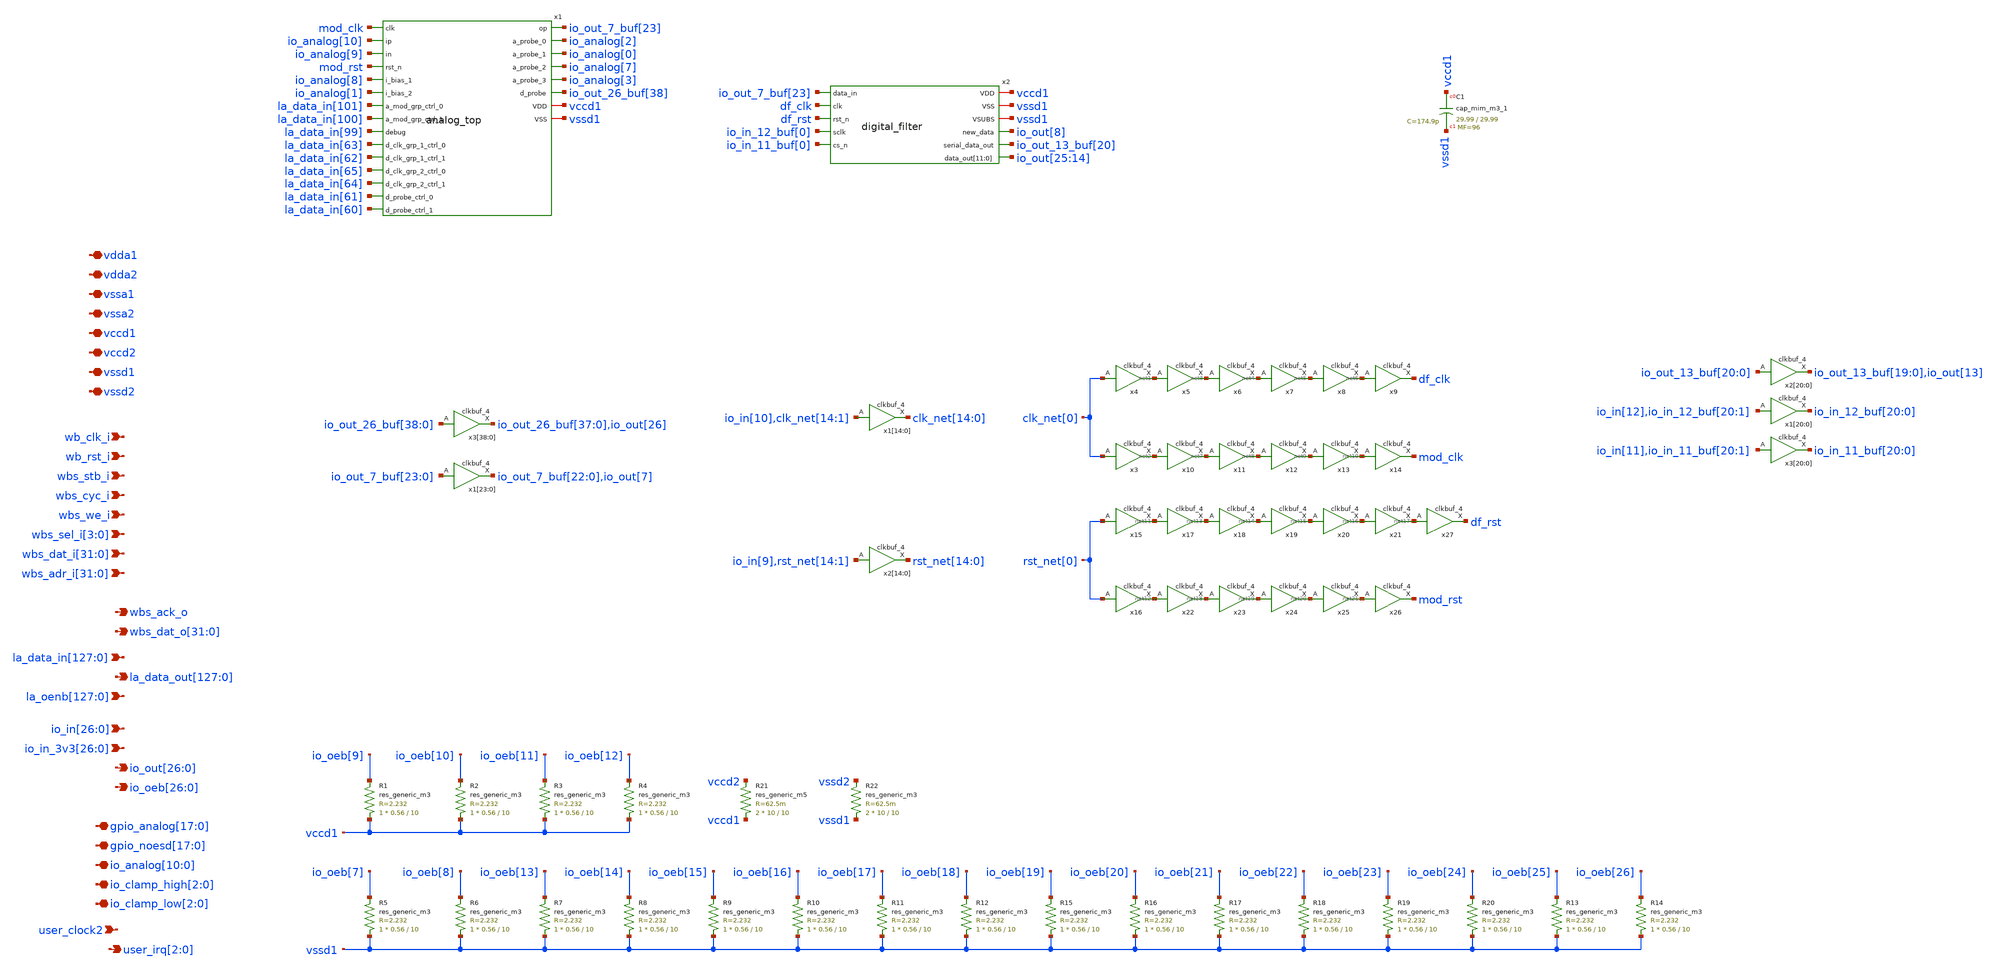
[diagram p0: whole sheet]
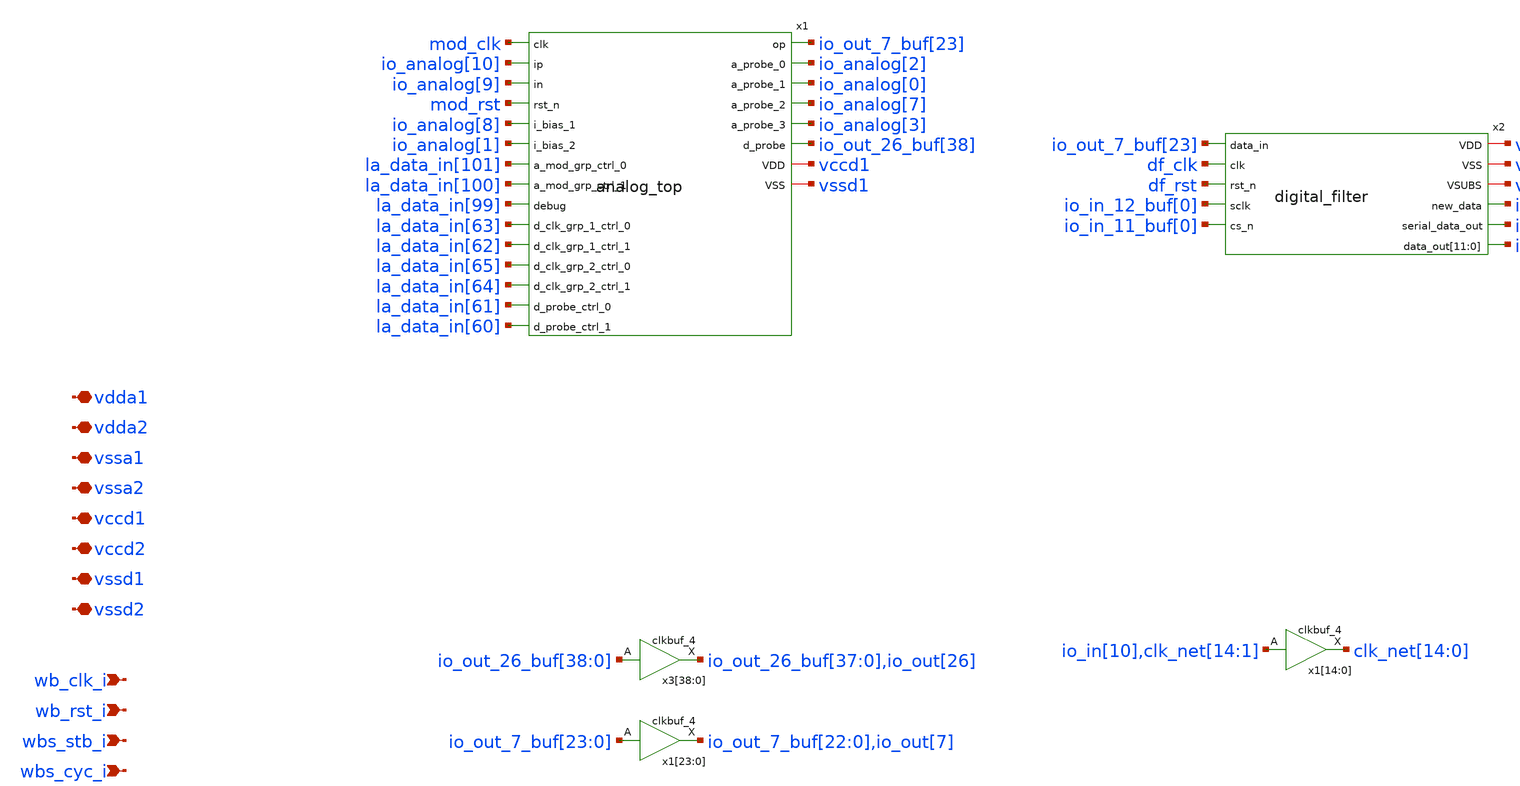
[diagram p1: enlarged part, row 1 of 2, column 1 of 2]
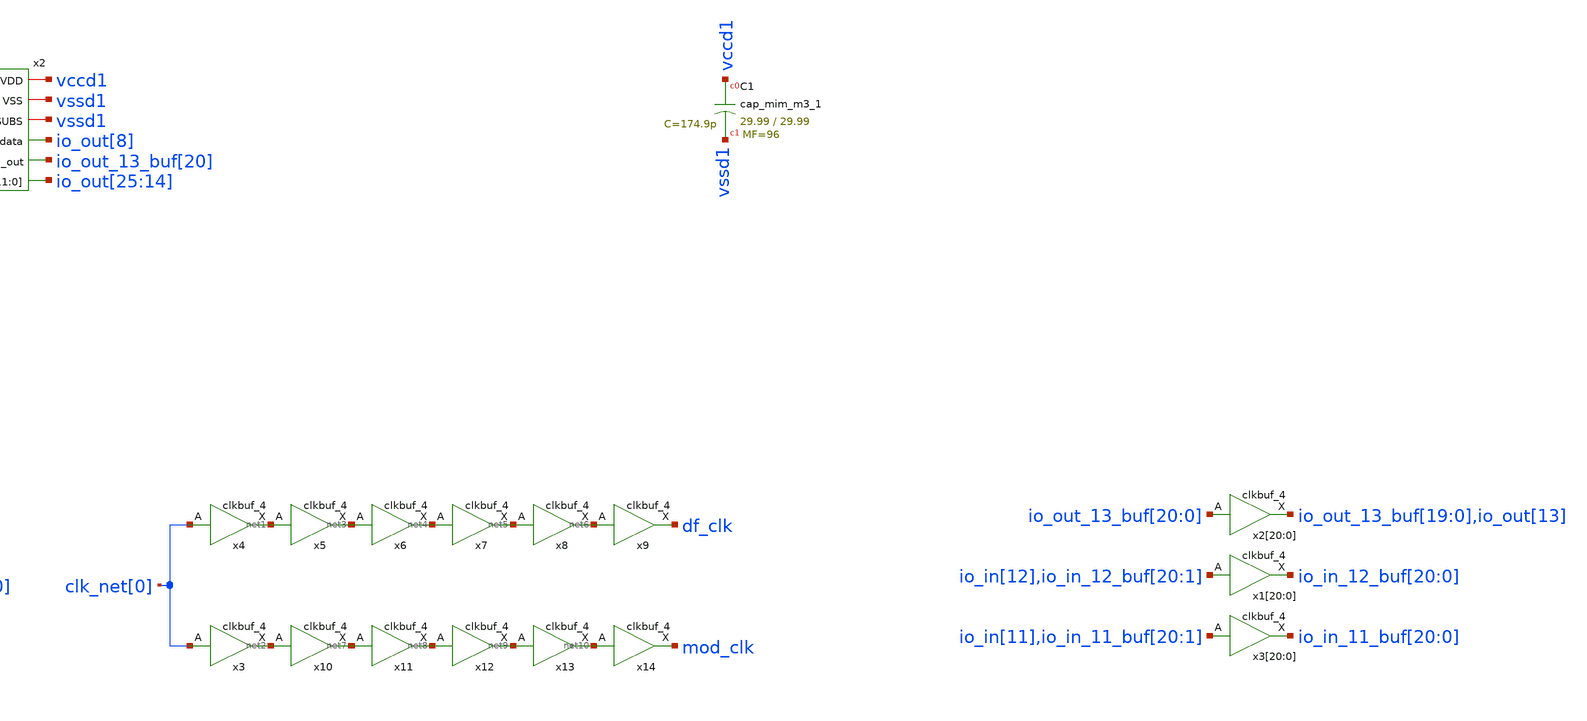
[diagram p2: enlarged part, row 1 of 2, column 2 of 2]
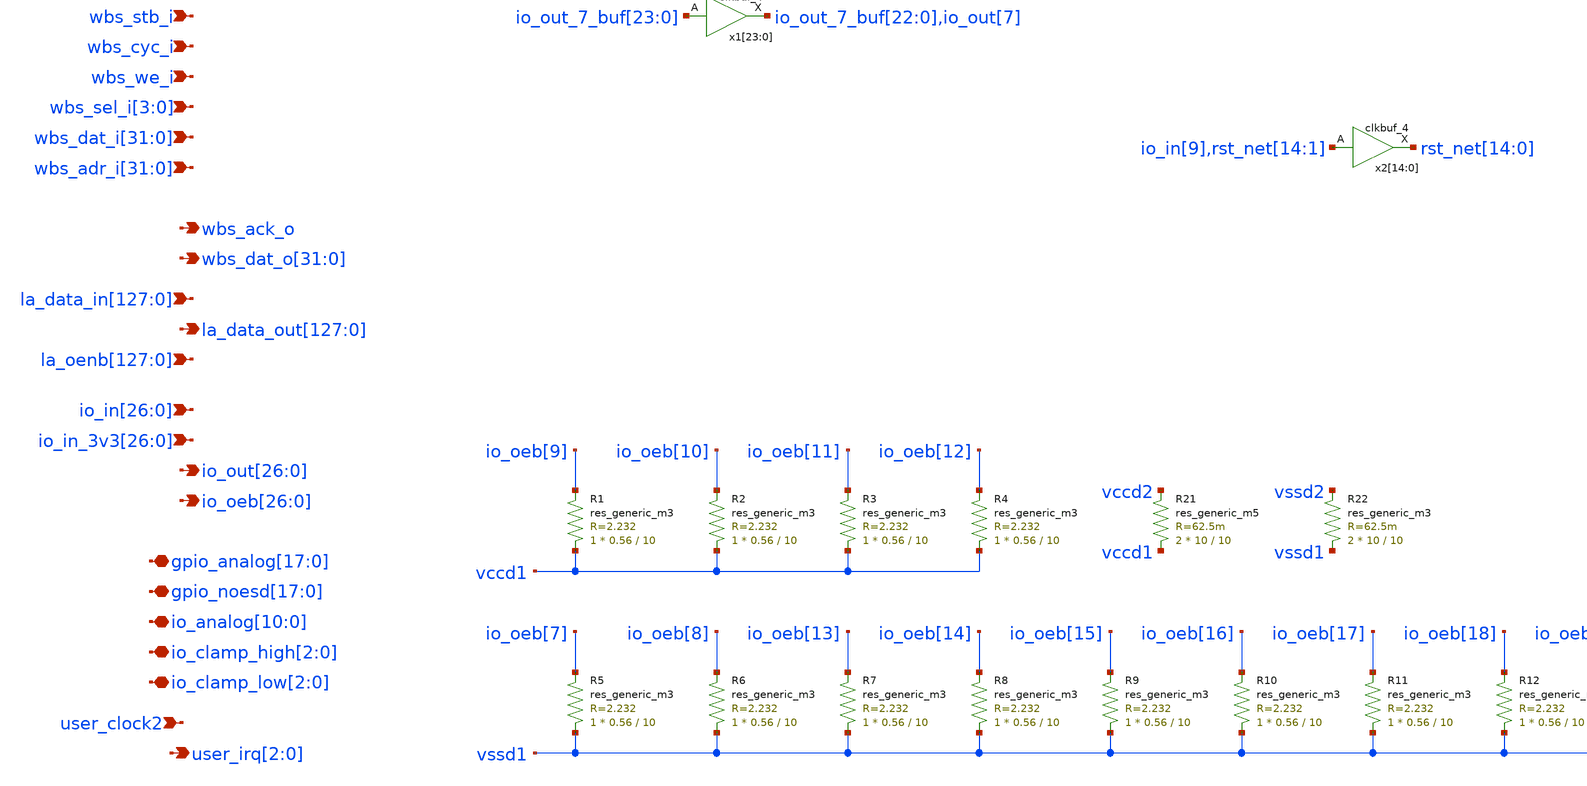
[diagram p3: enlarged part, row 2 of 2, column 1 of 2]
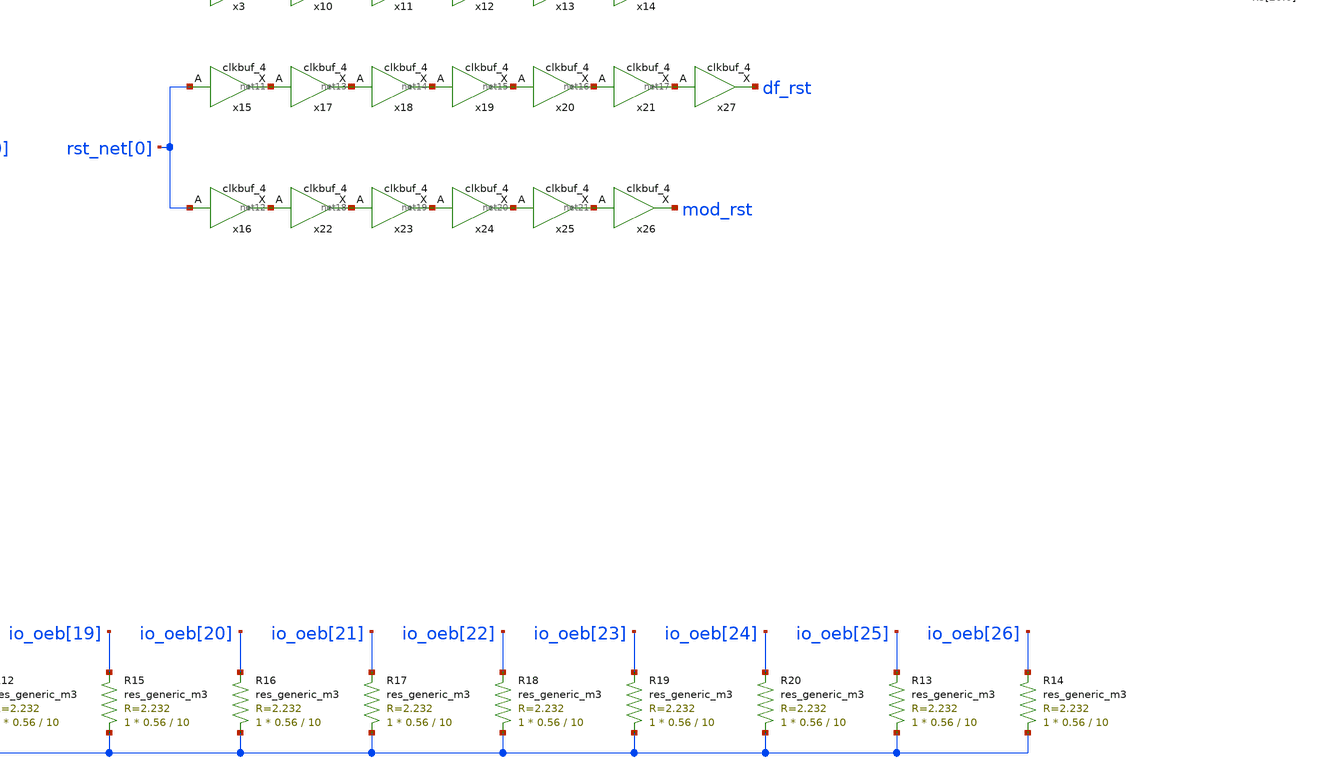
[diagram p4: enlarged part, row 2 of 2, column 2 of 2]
** sch_path: design/iadc_analog/user_analog_project_wrapper.sch
**.subckt user_analog_project_wrapper vdda1 vdda2 vssa1 vssa2 vccd1 vccd2 vssd1 vssd2 wb_clk_i
*+ wb_rst_i wbs_stb_i wbs_cyc_i wbs_we_i wbs_sel_i[3],wbs_sel_i[2],wbs_sel_i[1],wbs_sel_i[0]
*+ wbs_dat_i[31],wbs_dat_i[30],wbs_dat_i[29],wbs_dat_i[28],wbs_dat_i[27],wbs_dat_i[26],wbs_dat_i[25],wbs_dat_i[24],wbs_dat_i[23],wbs_dat_i[22],wbs_dat_i[21],wbs_dat_i[20],wbs_dat_i[19],wbs_dat_i[18],wbs_dat_i[17],wbs_dat_i[16],wbs_dat_i[15],wbs_dat_i[14],wbs_dat_i[13],wbs_dat_i[12],wbs_dat_i[11],wbs_dat_i[10],wbs_dat_i[9],wbs_dat_i[8],wbs_dat_i[7],wbs_dat_i[6],wbs_dat_i[5],wbs_dat_i[4],wbs_dat_i[3],wbs_dat_i[2],wbs_dat_i[1],wbs_dat_i[0]
*+ wbs_adr_i[31],wbs_adr_i[30],wbs_adr_i[29],wbs_adr_i[28],wbs_adr_i[27],wbs_adr_i[26],wbs_adr_i[25],wbs_adr_i[24],wbs_adr_i[23],wbs_adr_i[22],wbs_adr_i[21],wbs_adr_i[20],wbs_adr_i[19],wbs_adr_i[18],wbs_adr_i[17],wbs_adr_i[16],wbs_adr_i[15],wbs_adr_i[14],wbs_adr_i[13],wbs_adr_i[12],wbs_adr_i[11],wbs_adr_i[10],wbs_adr_i[9],wbs_adr_i[8],wbs_adr_i[7],wbs_adr_i[6],wbs_adr_i[5],wbs_adr_i[4],wbs_adr_i[3],wbs_adr_i[2],wbs_adr_i[1],wbs_adr_i[0] wbs_ack_o
*+ wbs_dat_o[31],wbs_dat_o[30],wbs_dat_o[29],wbs_dat_o[28],wbs_dat_o[27],wbs_dat_o[26],wbs_dat_o[25],wbs_dat_o[24],wbs_dat_o[23],wbs_dat_o[22],wbs_dat_o[21],wbs_dat_o[20],wbs_dat_o[19],wbs_dat_o[18],wbs_dat_o[17],wbs_dat_o[16],wbs_dat_o[15],wbs_dat_o[14],wbs_dat_o[13],wbs_dat_o[12],wbs_dat_o[11],wbs_dat_o[10],wbs_dat_o[9],wbs_dat_o[8],wbs_dat_o[7],wbs_dat_o[6],wbs_dat_o[5],wbs_dat_o[4],wbs_dat_o[3],wbs_dat_o[2],wbs_dat_o[1],wbs_dat_o[0]
*+ la_data_in[127],la_data_in[126],la_data_in[125],la_data_in[124],la_data_in[123],la_data_in[122],la_data_in[121],la_data_in[120],la_data_in[119],la_data_in[118],la_data_in[117],la_data_in[116],la_data_in[115],la_data_in[114],la_data_in[113],la_data_in[112],la_data_in[111],la_data_in[110],la_data_in[109],la_data_in[108],la_data_in[107],la_data_in[106],la_data_in[105],la_data_in[104],la_data_in[103],la_data_in[102],la_data_in[101],la_data_in[100],la_data_in[99],la_data_in[98],la_data_in[97],la_data_in[96],la_data_in[95],la_data_in[94],la_data_in[93],la_data_in[92],la_data_in[91],la_data_in[90],la_data_in[89],la_data_in[88],la_data_in[87],la_data_in[86],la_data_in[85],la_data_in[84],la_data_in[83],la_data_in[82],la_data_in[81],la_data_in[80],la_data_in[79],la_data_in[78],la_data_in[77],la_data_in[76],la_data_in[75],la_data_in[74],la_data_in[73],la_data_in[72],la_data_in[71],la_data_in[70],la_data_in[69],la_data_in[68],la_data_in[67],la_data_in[66],la_data_in[65],la_data_in[64],la_data_in[63],la_data_in[62],la_data_in[61],la_data_in[60],la_data_in[59],la_data_in[58],la_data_in[57],la_data_in[56],la_data_in[55],la_data_in[54],la_data_in[53],la_data_in[52],la_data_in[51],la_data_in[50],la_data_in[49],la_data_in[48],la_data_in[47],la_data_in[46],la_data_in[45],la_data_in[44],la_data_in[43],la_data_in[42],la_data_in[41],la_data_in[40],la_data_in[39],la_data_in[38],la_data_in[37],la_data_in[36],la_data_in[35],la_data_in[34],la_data_in[33],la_data_in[32],la_data_in[31],la_data_in[30],la_data_in[29],la_data_in[28],la_data_in[27],la_data_in[26],la_data_in[25],la_data_in[24],la_data_in[23],la_data_in[22],la_data_in[21],la_data_in[20],la_data_in[19],la_data_in[18],la_data_in[17],la_data_in[16],la_data_in[15],la_data_in[14],la_data_in[13],la_data_in[12],la_data_in[11],la_data_in[10],la_data_in[9],la_data_in[8],la_data_in[7],la_data_in[6],la_data_in[5],la_data_in[4],la_data_in[3],la_data_in[2],la_data_in[1],la_data_in[0]
*+ la_data_out[127],la_data_out[126],la_data_out[125],la_data_out[124],la_data_out[123],la_data_out[122],la_data_out[121],la_data_out[120],la_data_out[119],la_data_out[118],la_data_out[117],la_data_out[116],la_data_out[115],la_data_out[114],la_data_out[113],la_data_out[112],la_data_out[111],la_data_out[110],la_data_out[109],la_data_out[108],la_data_out[107],la_data_out[106],la_data_out[105],la_data_out[104],la_data_out[103],la_data_out[102],la_data_out[101],la_data_out[100],la_data_out[99],la_data_out[98],la_data_out[97],la_data_out[96],la_data_out[95],la_data_out[94],la_data_out[93],la_data_out[92],la_data_out[91],la_data_out[90],la_data_out[89],la_data_out[88],la_data_out[87],la_data_out[86],la_data_out[85],la_data_out[84],la_data_out[83],la_data_out[82],la_data_out[81],la_data_out[80],la_data_out[79],la_data_out[78],la_data_out[77],la_data_out[76],la_data_out[75],la_data_out[74],la_data_out[73],la_data_out[72],la_data_out[71],la_data_out[70],la_data_out[69],la_data_out[68],la_data_out[67],la_data_out[66],la_data_out[65],la_data_out[64],la_data_out[63],la_data_out[62],la_data_out[61],la_data_out[60],la_data_out[59],la_data_out[58],la_data_out[57],la_data_out[56],la_data_out[55],la_data_out[54],la_data_out[53],la_data_out[52],la_data_out[51],la_data_out[50],la_data_out[49],la_data_out[48],la_data_out[47],la_data_out[46],la_data_out[45],la_data_out[44],la_data_out[43],la_data_out[42],la_data_out[41],la_data_out[40],la_data_out[39],la_data_out[38],la_data_out[37],la_data_out[36],la_data_out[35],la_data_out[34],la_data_out[33],la_data_out[32],la_data_out[31],la_data_out[30],la_data_out[29],la_data_out[28],la_data_out[27],la_data_out[26],la_data_out[25],la_data_out[24],la_data_out[23],la_data_out[22],la_data_out[21],la_data_out[20],la_data_out[19],la_data_out[18],la_data_out[17],la_data_out[16],la_data_out[15],la_data_out[14],la_data_out[13],la_data_out[12],la_data_out[11],la_data_out[10],la_data_out[9],la_data_out[8],la_data_out[7],la_data_out[6],la_data_out[5],la_data_out[4],la_data_out[3],la_data_out[2],la_data_out[1],la_data_out[0]
*+ io_in[26],io_in[25],io_in[24],io_in[23],io_in[22],io_in[21],io_in[20],io_in[19],io_in[18],io_in[17],io_in[16],io_in[15],io_in[14],io_in[13],io_in[12],io_in[11],io_in[10],io_in[9],io_in[8],io_in[7],io_in[6],io_in[5],io_in[4],io_in[3],io_in[2],io_in[1],io_in[0]
*+ io_in_3v3[26],io_in_3v3[25],io_in_3v3[24],io_in_3v3[23],io_in_3v3[22],io_in_3v3[21],io_in_3v3[20],io_in_3v3[19],io_in_3v3[18],io_in_3v3[17],io_in_3v3[16],io_in_3v3[15],io_in_3v3[14],io_in_3v3[13],io_in_3v3[12],io_in_3v3[11],io_in_3v3[10],io_in_3v3[9],io_in_3v3[8],io_in_3v3[7],io_in_3v3[6],io_in_3v3[5],io_in_3v3[4],io_in_3v3[3],io_in_3v3[2],io_in_3v3[1],io_in_3v3[0] user_clock2
*+ io_out[26],io_out[25],io_out[24],io_out[23],io_out[22],io_out[21],io_out[20],io_out[19],io_out[18],io_out[17],io_out[16],io_out[15],io_out[14],io_out[13],io_out[12],io_out[11],io_out[10],io_out[9],io_out[8],io_out[7],io_out[6],io_out[5],io_out[4],io_out[3],io_out[2],io_out[1],io_out[0]
*+ io_oeb[26],io_oeb[25],io_oeb[24],io_oeb[23],io_oeb[22],io_oeb[21],io_oeb[20],io_oeb[19],io_oeb[18],io_oeb[17],io_oeb[16],io_oeb[15],io_oeb[14],io_oeb[13],io_oeb[12],io_oeb[11],io_oeb[10],io_oeb[9],io_oeb[8],io_oeb[7],io_oeb[6],io_oeb[5],io_oeb[4],io_oeb[3],io_oeb[2],io_oeb[1],io_oeb[0]
*+ gpio_analog[17],gpio_analog[16],gpio_analog[15],gpio_analog[14],gpio_analog[13],gpio_analog[12],gpio_analog[11],gpio_analog[10],gpio_analog[9],gpio_analog[8],gpio_analog[7],gpio_analog[6],gpio_analog[5],gpio_analog[4],gpio_analog[3],gpio_analog[2],gpio_analog[1],gpio_analog[0]
*+ gpio_noesd[17],gpio_noesd[16],gpio_noesd[15],gpio_noesd[14],gpio_noesd[13],gpio_noesd[12],gpio_noesd[11],gpio_noesd[10],gpio_noesd[9],gpio_noesd[8],gpio_noesd[7],gpio_noesd[6],gpio_noesd[5],gpio_noesd[4],gpio_noesd[3],gpio_noesd[2],gpio_noesd[1],gpio_noesd[0]
*+ io_analog[10],io_analog[9],io_analog[8],io_analog[7],io_analog[6],io_analog[5],io_analog[4],io_analog[3],io_analog[2],io_analog[1],io_analog[0] io_clamp_high[2],io_clamp_high[1],io_clamp_high[0] io_clamp_low[2],io_clamp_low[1],io_clamp_low[0]
*+ user_irq[2],user_irq[1],user_irq[0]
*+ la_oenb[127],la_oenb[126],la_oenb[125],la_oenb[124],la_oenb[123],la_oenb[122],la_oenb[121],la_oenb[120],la_oenb[119],la_oenb[118],la_oenb[117],la_oenb[116],la_oenb[115],la_oenb[114],la_oenb[113],la_oenb[112],la_oenb[111],la_oenb[110],la_oenb[109],la_oenb[108],la_oenb[107],la_oenb[106],la_oenb[105],la_oenb[104],la_oenb[103],la_oenb[102],la_oenb[101],la_oenb[100],la_oenb[99],la_oenb[98],la_oenb[97],la_oenb[96],la_oenb[95],la_oenb[94],la_oenb[93],la_oenb[92],la_oenb[91],la_oenb[90],la_oenb[89],la_oenb[88],la_oenb[87],la_oenb[86],la_oenb[85],la_oenb[84],la_oenb[83],la_oenb[82],la_oenb[81],la_oenb[80],la_oenb[79],la_oenb[78],la_oenb[77],la_oenb[76],la_oenb[75],la_oenb[74],la_oenb[73],la_oenb[72],la_oenb[71],la_oenb[70],la_oenb[69],la_oenb[68],la_oenb[67],la_oenb[66],la_oenb[65],la_oenb[64],la_oenb[63],la_oenb[62],la_oenb[61],la_oenb[60],la_oenb[59],la_oenb[58],la_oenb[57],la_oenb[56],la_oenb[55],la_oenb[54],la_oenb[53],la_oenb[52],la_oenb[51],la_oenb[50],la_oenb[49],la_oenb[48],la_oenb[47],la_oenb[46],la_oenb[45],la_oenb[44],la_oenb[43],la_oenb[42],la_oenb[41],la_oenb[40],la_oenb[39],la_oenb[38],la_oenb[37],la_oenb[36],la_oenb[35],la_oenb[34],la_oenb[33],la_oenb[32],la_oenb[31],la_oenb[30],la_oenb[29],la_oenb[28],la_oenb[27],la_oenb[26],la_oenb[25],la_oenb[24],la_oenb[23],la_oenb[22],la_oenb[21],la_oenb[20],la_oenb[19],la_oenb[18],la_oenb[17],la_oenb[16],la_oenb[15],la_oenb[14],la_oenb[13],la_oenb[12],la_oenb[11],la_oenb[10],la_oenb[9],la_oenb[8],la_oenb[7],la_oenb[6],la_oenb[5],la_oenb[4],la_oenb[3],la_oenb[2],la_oenb[1],la_oenb[0]
*.iopin vdda1
*.iopin vdda2
*.iopin vssa1
*.iopin vssa2
*.iopin vccd1
*.iopin vccd2
*.iopin vssd1
*.iopin vssd2
*.ipin wb_clk_i
*.ipin wb_rst_i
*.ipin wbs_stb_i
*.ipin wbs_cyc_i
*.ipin wbs_we_i
*.ipin wbs_sel_i[3],wbs_sel_i[2],wbs_sel_i[1],wbs_sel_i[0]
*.ipin
*+ wbs_dat_i[31],wbs_dat_i[30],wbs_dat_i[29],wbs_dat_i[28],wbs_dat_i[27],wbs_dat_i[26],wbs_dat_i[25],wbs_dat_i[24],wbs_dat_i[23],wbs_dat_i[22],wbs_dat_i[21],wbs_dat_i[20],wbs_dat_i[19],wbs_dat_i[18],wbs_dat_i[17],wbs_dat_i[16],wbs_dat_i[15],wbs_dat_i[14],wbs_dat_i[13],wbs_dat_i[12],wbs_dat_i[11],wbs_dat_i[10],wbs_dat_i[9],wbs_dat_i[8],wbs_dat_i[7],wbs_dat_i[6],wbs_dat_i[5],wbs_dat_i[4],wbs_dat_i[3],wbs_dat_i[2],wbs_dat_i[1],wbs_dat_i[0]
*.ipin
*+ wbs_adr_i[31],wbs_adr_i[30],wbs_adr_i[29],wbs_adr_i[28],wbs_adr_i[27],wbs_adr_i[26],wbs_adr_i[25],wbs_adr_i[24],wbs_adr_i[23],wbs_adr_i[22],wbs_adr_i[21],wbs_adr_i[20],wbs_adr_i[19],wbs_adr_i[18],wbs_adr_i[17],wbs_adr_i[16],wbs_adr_i[15],wbs_adr_i[14],wbs_adr_i[13],wbs_adr_i[12],wbs_adr_i[11],wbs_adr_i[10],wbs_adr_i[9],wbs_adr_i[8],wbs_adr_i[7],wbs_adr_i[6],wbs_adr_i[5],wbs_adr_i[4],wbs_adr_i[3],wbs_adr_i[2],wbs_adr_i[1],wbs_adr_i[0]
*.opin wbs_ack_o
*.opin
*+ wbs_dat_o[31],wbs_dat_o[30],wbs_dat_o[29],wbs_dat_o[28],wbs_dat_o[27],wbs_dat_o[26],wbs_dat_o[25],wbs_dat_o[24],wbs_dat_o[23],wbs_dat_o[22],wbs_dat_o[21],wbs_dat_o[20],wbs_dat_o[19],wbs_dat_o[18],wbs_dat_o[17],wbs_dat_o[16],wbs_dat_o[15],wbs_dat_o[14],wbs_dat_o[13],wbs_dat_o[12],wbs_dat_o[11],wbs_dat_o[10],wbs_dat_o[9],wbs_dat_o[8],wbs_dat_o[7],wbs_dat_o[6],wbs_dat_o[5],wbs_dat_o[4],wbs_dat_o[3],wbs_dat_o[2],wbs_dat_o[1],wbs_dat_o[0]
*.ipin
*+ la_data_in[127],la_data_in[126],la_data_in[125],la_data_in[124],la_data_in[123],la_data_in[122],la_data_in[121],la_data_in[120],la_data_in[119],la_data_in[118],la_data_in[117],la_data_in[116],la_data_in[115],la_data_in[114],la_data_in[113],la_data_in[112],la_data_in[111],la_data_in[110],la_data_in[109],la_data_in[108],la_data_in[107],la_data_in[106],la_data_in[105],la_data_in[104],la_data_in[103],la_data_in[102],la_data_in[101],la_data_in[100],la_data_in[99],la_data_in[98],la_data_in[97],la_data_in[96],la_data_in[95],la_data_in[94],la_data_in[93],la_data_in[92],la_data_in[91],la_data_in[90],la_data_in[89],la_data_in[88],la_data_in[87],la_data_in[86],la_data_in[85],la_data_in[84],la_data_in[83],la_data_in[82],la_data_in[81],la_data_in[80],la_data_in[79],la_data_in[78],la_data_in[77],la_data_in[76],la_data_in[75],la_data_in[74],la_data_in[73],la_data_in[72],la_data_in[71],la_data_in[70],la_data_in[69],la_data_in[68],la_data_in[67],la_data_in[66],la_data_in[65],la_data_in[64],la_data_in[63],la_data_in[62],la_data_in[61],la_data_in[60],la_data_in[59],la_data_in[58],la_data_in[57],la_data_in[56],la_data_in[55],la_data_in[54],la_data_in[53],la_data_in[52],la_data_in[51],la_data_in[50],la_data_in[49],la_data_in[48],la_data_in[47],la_data_in[46],la_data_in[45],la_data_in[44],la_data_in[43],la_data_in[42],la_data_in[41],la_data_in[40],la_data_in[39],la_data_in[38],la_data_in[37],la_data_in[36],la_data_in[35],la_data_in[34],la_data_in[33],la_data_in[32],la_data_in[31],la_data_in[30],la_data_in[29],la_data_in[28],la_data_in[27],la_data_in[26],la_data_in[25],la_data_in[24],la_data_in[23],la_data_in[22],la_data_in[21],la_data_in[20],la_data_in[19],la_data_in[18],la_data_in[17],la_data_in[16],la_data_in[15],la_data_in[14],la_data_in[13],la_data_in[12],la_data_in[11],la_data_in[10],la_data_in[9],la_data_in[8],la_data_in[7],la_data_in[6],la_data_in[5],la_data_in[4],la_data_in[3],la_data_in[2],la_data_in[1],la_data_in[0]
*.opin
*+ la_data_out[127],la_data_out[126],la_data_out[125],la_data_out[124],la_data_out[123],la_data_out[122],la_data_out[121],la_data_out[120],la_data_out[119],la_data_out[118],la_data_out[117],la_data_out[116],la_data_out[115],la_data_out[114],la_data_out[113],la_data_out[112],la_data_out[111],la_data_out[110],la_data_out[109],la_data_out[108],la_data_out[107],la_data_out[106],la_data_out[105],la_data_out[104],la_data_out[103],la_data_out[102],la_data_out[101],la_data_out[100],la_data_out[99],la_data_out[98],la_data_out[97],la_data_out[96],la_data_out[95],la_data_out[94],la_data_out[93],la_data_out[92],la_data_out[91],la_data_out[90],la_data_out[89],la_data_out[88],la_data_out[87],la_data_out[86],la_data_out[85],la_data_out[84],la_data_out[83],la_data_out[82],la_data_out[81],la_data_out[80],la_data_out[79],la_data_out[78],la_data_out[77],la_data_out[76],la_data_out[75],la_data_out[74],la_data_out[73],la_data_out[72],la_data_out[71],la_data_out[70],la_data_out[69],la_data_out[68],la_data_out[67],la_data_out[66],la_data_out[65],la_data_out[64],la_data_out[63],la_data_out[62],la_data_out[61],la_data_out[60],la_data_out[59],la_data_out[58],la_data_out[57],la_data_out[56],la_data_out[55],la_data_out[54],la_data_out[53],la_data_out[52],la_data_out[51],la_data_out[50],la_data_out[49],la_data_out[48],la_data_out[47],la_data_out[46],la_data_out[45],la_data_out[44],la_data_out[43],la_data_out[42],la_data_out[41],la_data_out[40],la_data_out[39],la_data_out[38],la_data_out[37],la_data_out[36],la_data_out[35],la_data_out[34],la_data_out[33],la_data_out[32],la_data_out[31],la_data_out[30],la_data_out[29],la_data_out[28],la_data_out[27],la_data_out[26],la_data_out[25],la_data_out[24],la_data_out[23],la_data_out[22],la_data_out[21],la_data_out[20],la_data_out[19],la_data_out[18],la_data_out[17],la_data_out[16],la_data_out[15],la_data_out[14],la_data_out[13],la_data_out[12],la_data_out[11],la_data_out[10],la_data_out[9],la_data_out[8],la_data_out[7],la_data_out[6],la_data_out[5],la_data_out[4],la_data_out[3],la_data_out[2],la_data_out[1],la_data_out[0]
*.ipin
*+ io_in[26],io_in[25],io_in[24],io_in[23],io_in[22],io_in[21],io_in[20],io_in[19],io_in[18],io_in[17],io_in[16],io_in[15],io_in[14],io_in[13],io_in[12],io_in[11],io_in[10],io_in[9],io_in[8],io_in[7],io_in[6],io_in[5],io_in[4],io_in[3],io_in[2],io_in[1],io_in[0]
*.ipin
*+ io_in_3v3[26],io_in_3v3[25],io_in_3v3[24],io_in_3v3[23],io_in_3v3[22],io_in_3v3[21],io_in_3v3[20],io_in_3v3[19],io_in_3v3[18],io_in_3v3[17],io_in_3v3[16],io_in_3v3[15],io_in_3v3[14],io_in_3v3[13],io_in_3v3[12],io_in_3v3[11],io_in_3v3[10],io_in_3v3[9],io_in_3v3[8],io_in_3v3[7],io_in_3v3[6],io_in_3v3[5],io_in_3v3[4],io_in_3v3[3],io_in_3v3[2],io_in_3v3[1],io_in_3v3[0]
*.ipin user_clock2
*.opin
*+ io_out[26],io_out[25],io_out[24],io_out[23],io_out[22],io_out[21],io_out[20],io_out[19],io_out[18],io_out[17],io_out[16],io_out[15],io_out[14],io_out[13],io_out[12],io_out[11],io_out[10],io_out[9],io_out[8],io_out[7],io_out[6],io_out[5],io_out[4],io_out[3],io_out[2],io_out[1],io_out[0]
*.opin
*+ io_oeb[26],io_oeb[25],io_oeb[24],io_oeb[23],io_oeb[22],io_oeb[21],io_oeb[20],io_oeb[19],io_oeb[18],io_oeb[17],io_oeb[16],io_oeb[15],io_oeb[14],io_oeb[13],io_oeb[12],io_oeb[11],io_oeb[10],io_oeb[9],io_oeb[8],io_oeb[7],io_oeb[6],io_oeb[5],io_oeb[4],io_oeb[3],io_oeb[2],io_oeb[1],io_oeb[0]
*.iopin
*+ gpio_analog[17],gpio_analog[16],gpio_analog[15],gpio_analog[14],gpio_analog[13],gpio_analog[12],gpio_analog[11],gpio_analog[10],gpio_analog[9],gpio_analog[8],gpio_analog[7],gpio_analog[6],gpio_analog[5],gpio_analog[4],gpio_analog[3],gpio_analog[2],gpio_analog[1],gpio_analog[0]
*.iopin
*+ gpio_noesd[17],gpio_noesd[16],gpio_noesd[15],gpio_noesd[14],gpio_noesd[13],gpio_noesd[12],gpio_noesd[11],gpio_noesd[10],gpio_noesd[9],gpio_noesd[8],gpio_noesd[7],gpio_noesd[6],gpio_noesd[5],gpio_noesd[4],gpio_noesd[3],gpio_noesd[2],gpio_noesd[1],gpio_noesd[0]
*.iopin
*+ io_analog[10],io_analog[9],io_analog[8],io_analog[7],io_analog[6],io_analog[5],io_analog[4],io_analog[3],io_analog[2],io_analog[1],io_analog[0]
*.iopin io_clamp_high[2],io_clamp_high[1],io_clamp_high[0]
*.iopin io_clamp_low[2],io_clamp_low[1],io_clamp_low[0]
*.opin user_irq[2],user_irq[1],user_irq[0]
*.ipin
*+ la_oenb[127],la_oenb[126],la_oenb[125],la_oenb[124],la_oenb[123],la_oenb[122],la_oenb[121],la_oenb[120],la_oenb[119],la_oenb[118],la_oenb[117],la_oenb[116],la_oenb[115],la_oenb[114],la_oenb[113],la_oenb[112],la_oenb[111],la_oenb[110],la_oenb[109],la_oenb[108],la_oenb[107],la_oenb[106],la_oenb[105],la_oenb[104],la_oenb[103],la_oenb[102],la_oenb[101],la_oenb[100],la_oenb[99],la_oenb[98],la_oenb[97],la_oenb[96],la_oenb[95],la_oenb[94],la_oenb[93],la_oenb[92],la_oenb[91],la_oenb[90],la_oenb[89],la_oenb[88],la_oenb[87],la_oenb[86],la_oenb[85],la_oenb[84],la_oenb[83],la_oenb[82],la_oenb[81],la_oenb[80],la_oenb[79],la_oenb[78],la_oenb[77],la_oenb[76],la_oenb[75],la_oenb[74],la_oenb[73],la_oenb[72],la_oenb[71],la_oenb[70],la_oenb[69],la_oenb[68],la_oenb[67],la_oenb[66],la_oenb[65],la_oenb[64],la_oenb[63],la_oenb[62],la_oenb[61],la_oenb[60],la_oenb[59],la_oenb[58],la_oenb[57],la_oenb[56],la_oenb[55],la_oenb[54],la_oenb[53],la_oenb[52],la_oenb[51],la_oenb[50],la_oenb[49],la_oenb[48],la_oenb[47],la_oenb[46],la_oenb[45],la_oenb[44],la_oenb[43],la_oenb[42],la_oenb[41],la_oenb[40],la_oenb[39],la_oenb[38],la_oenb[37],la_oenb[36],la_oenb[35],la_oenb[34],la_oenb[33],la_oenb[32],la_oenb[31],la_oenb[30],la_oenb[29],la_oenb[28],la_oenb[27],la_oenb[26],la_oenb[25],la_oenb[24],la_oenb[23],la_oenb[22],la_oenb[21],la_oenb[20],la_oenb[19],la_oenb[18],la_oenb[17],la_oenb[16],la_oenb[15],la_oenb[14],la_oenb[13],la_oenb[12],la_oenb[11],la_oenb[10],la_oenb[9],la_oenb[8],la_oenb[7],la_oenb[6],la_oenb[5],la_oenb[4],la_oenb[3],la_oenb[2],la_oenb[1],la_oenb[0]
R1 vccd1 io_oeb[9] sky130_fd_pr__res_generic_m3 W=0.56 L=10 m=1
R2 vccd1 io_oeb[10] sky130_fd_pr__res_generic_m3 W=0.56 L=10 m=1
R3 vccd1 io_oeb[11] sky130_fd_pr__res_generic_m3 W=0.56 L=10 m=1
R4 vccd1 io_oeb[12] sky130_fd_pr__res_generic_m3 W=0.56 L=10 m=1
R5 vssd1 io_oeb[7] sky130_fd_pr__res_generic_m3 W=0.56 L=10 m=1
R6 vssd1 io_oeb[8] sky130_fd_pr__res_generic_m3 W=0.56 L=10 m=1
R7 vssd1 io_oeb[13] sky130_fd_pr__res_generic_m3 W=0.56 L=10 m=1
R8 vssd1 io_oeb[14] sky130_fd_pr__res_generic_m3 W=0.56 L=10 m=1
R9 vssd1 io_oeb[15] sky130_fd_pr__res_generic_m3 W=0.56 L=10 m=1
R10 vssd1 io_oeb[16] sky130_fd_pr__res_generic_m3 W=0.56 L=10 m=1
R11 vssd1 io_oeb[17] sky130_fd_pr__res_generic_m3 W=0.56 L=10 m=1
R12 vssd1 io_oeb[18] sky130_fd_pr__res_generic_m3 W=0.56 L=10 m=1
R13 vssd1 io_oeb[25] sky130_fd_pr__res_generic_m3 W=0.56 L=10 m=1
R14 vssd1 io_oeb[26] sky130_fd_pr__res_generic_m3 W=0.56 L=10 m=1
R15 vssd1 io_oeb[19] sky130_fd_pr__res_generic_m3 W=0.56 L=10 m=1
R16 vssd1 io_oeb[20] sky130_fd_pr__res_generic_m3 W=0.56 L=10 m=1
R17 vssd1 io_oeb[21] sky130_fd_pr__res_generic_m3 W=0.56 L=10 m=1
R18 vssd1 io_oeb[22] sky130_fd_pr__res_generic_m3 W=0.56 L=10 m=1
R19 vssd1 io_oeb[23] sky130_fd_pr__res_generic_m3 W=0.56 L=10 m=1
R20 vssd1 io_oeb[24] sky130_fd_pr__res_generic_m3 W=0.56 L=10 m=1
x2 vccd1 vssd1 vssd1 io_out_7_buf[23] df_clk df_rst io_in_12_buf[0] io_in_11_buf[0] io_out[8]
+ io_out_13_buf[20] io_out[25] io_out[24] io_out[23] io_out[22] io_out[21] io_out[20] io_out[19] io_out[18] io_out[17]
+ io_out[16] io_out[15] io_out[14] digital_filter
R21 vccd1 vccd2 sky130_fd_pr__res_generic_m5 W=10 L=10 m=2
R22 vssd1 vssd2 sky130_fd_pr__res_generic_m3 W=10 L=10 m=2
x3[38] io_out_26_buf[38] vssd1 vssd1 vccd1 vccd1 io_out_26_buf[37] sky130_fd_sc_hd__clkbuf_4
x3[37] io_out_26_buf[37] vssd1 vssd1 vccd1 vccd1 io_out_26_buf[36] sky130_fd_sc_hd__clkbuf_4
x3[36] io_out_26_buf[36] vssd1 vssd1 vccd1 vccd1 io_out_26_buf[35] sky130_fd_sc_hd__clkbuf_4
x3[35] io_out_26_buf[35] vssd1 vssd1 vccd1 vccd1 io_out_26_buf[34] sky130_fd_sc_hd__clkbuf_4
x3[34] io_out_26_buf[34] vssd1 vssd1 vccd1 vccd1 io_out_26_buf[33] sky130_fd_sc_hd__clkbuf_4
x3[33] io_out_26_buf[33] vssd1 vssd1 vccd1 vccd1 io_out_26_buf[32] sky130_fd_sc_hd__clkbuf_4
x3[32] io_out_26_buf[32] vssd1 vssd1 vccd1 vccd1 io_out_26_buf[31] sky130_fd_sc_hd__clkbuf_4
x3[31] io_out_26_buf[31] vssd1 vssd1 vccd1 vccd1 io_out_26_buf[30] sky130_fd_sc_hd__clkbuf_4
x3[30] io_out_26_buf[30] vssd1 vssd1 vccd1 vccd1 io_out_26_buf[29] sky130_fd_sc_hd__clkbuf_4
x3[29] io_out_26_buf[29] vssd1 vssd1 vccd1 vccd1 io_out_26_buf[28] sky130_fd_sc_hd__clkbuf_4
x3[28] io_out_26_buf[28] vssd1 vssd1 vccd1 vccd1 io_out_26_buf[27] sky130_fd_sc_hd__clkbuf_4
x3[27] io_out_26_buf[27] vssd1 vssd1 vccd1 vccd1 io_out_26_buf[26] sky130_fd_sc_hd__clkbuf_4
x3[26] io_out_26_buf[26] vssd1 vssd1 vccd1 vccd1 io_out_26_buf[25] sky130_fd_sc_hd__clkbuf_4
x3[25] io_out_26_buf[25] vssd1 vssd1 vccd1 vccd1 io_out_26_buf[24] sky130_fd_sc_hd__clkbuf_4
x3[24] io_out_26_buf[24] vssd1 vssd1 vccd1 vccd1 io_out_26_buf[23] sky130_fd_sc_hd__clkbuf_4
x3[23] io_out_26_buf[23] vssd1 vssd1 vccd1 vccd1 io_out_26_buf[22] sky130_fd_sc_hd__clkbuf_4
x3[22] io_out_26_buf[22] vssd1 vssd1 vccd1 vccd1 io_out_26_buf[21] sky130_fd_sc_hd__clkbuf_4
x3[21] io_out_26_buf[21] vssd1 vssd1 vccd1 vccd1 io_out_26_buf[20] sky130_fd_sc_hd__clkbuf_4
x3[20] io_out_26_buf[20] vssd1 vssd1 vccd1 vccd1 io_out_26_buf[19] sky130_fd_sc_hd__clkbuf_4
x3[19] io_out_26_buf[19] vssd1 vssd1 vccd1 vccd1 io_out_26_buf[18] sky130_fd_sc_hd__clkbuf_4
x3[18] io_out_26_buf[18] vssd1 vssd1 vccd1 vccd1 io_out_26_buf[17] sky130_fd_sc_hd__clkbuf_4
x3[17] io_out_26_buf[17] vssd1 vssd1 vccd1 vccd1 io_out_26_buf[16] sky130_fd_sc_hd__clkbuf_4
x3[16] io_out_26_buf[16] vssd1 vssd1 vccd1 vccd1 io_out_26_buf[15] sky130_fd_sc_hd__clkbuf_4
x3[15] io_out_26_buf[15] vssd1 vssd1 vccd1 vccd1 io_out_26_buf[14] sky130_fd_sc_hd__clkbuf_4
x3[14] io_out_26_buf[14] vssd1 vssd1 vccd1 vccd1 io_out_26_buf[13] sky130_fd_sc_hd__clkbuf_4
x3[13] io_out_26_buf[13] vssd1 vssd1 vccd1 vccd1 io_out_26_buf[12] sky130_fd_sc_hd__clkbuf_4
x3[12] io_out_26_buf[12] vssd1 vssd1 vccd1 vccd1 io_out_26_buf[11] sky130_fd_sc_hd__clkbuf_4
x3[11] io_out_26_buf[11] vssd1 vssd1 vccd1 vccd1 io_out_26_buf[10] sky130_fd_sc_hd__clkbuf_4
x3[10] io_out_26_buf[10] vssd1 vssd1 vccd1 vccd1 io_out_26_buf[9] sky130_fd_sc_hd__clkbuf_4
x3[9] io_out_26_buf[9] vssd1 vssd1 vccd1 vccd1 io_out_26_buf[8] sky130_fd_sc_hd__clkbuf_4
x3[8] io_out_26_buf[8] vssd1 vssd1 vccd1 vccd1 io_out_26_buf[7] sky130_fd_sc_hd__clkbuf_4
x3[7] io_out_26_buf[7] vssd1 vssd1 vccd1 vccd1 io_out_26_buf[6] sky130_fd_sc_hd__clkbuf_4
x3[6] io_out_26_buf[6] vssd1 vssd1 vccd1 vccd1 io_out_26_buf[5] sky130_fd_sc_hd__clkbuf_4
x3[5] io_out_26_buf[5] vssd1 vssd1 vccd1 vccd1 io_out_26_buf[4] sky130_fd_sc_hd__clkbuf_4
x3[4] io_out_26_buf[4] vssd1 vssd1 vccd1 vccd1 io_out_26_buf[3] sky130_fd_sc_hd__clkbuf_4
x3[3] io_out_26_buf[3] vssd1 vssd1 vccd1 vccd1 io_out_26_buf[2] sky130_fd_sc_hd__clkbuf_4
x3[2] io_out_26_buf[2] vssd1 vssd1 vccd1 vccd1 io_out_26_buf[1] sky130_fd_sc_hd__clkbuf_4
x3[1] io_out_26_buf[1] vssd1 vssd1 vccd1 vccd1 io_out_26_buf[0] sky130_fd_sc_hd__clkbuf_4
x3[0] io_out_26_buf[0] vssd1 vssd1 vccd1 vccd1 io_out[26] sky130_fd_sc_hd__clkbuf_4
x1[23] io_out_7_buf[23] vssd1 vssd1 vccd1 vccd1 io_out_7_buf[22] sky130_fd_sc_hd__clkbuf_4
x1[22] io_out_7_buf[22] vssd1 vssd1 vccd1 vccd1 io_out_7_buf[21] sky130_fd_sc_hd__clkbuf_4
x1[21] io_out_7_buf[21] vssd1 vssd1 vccd1 vccd1 io_out_7_buf[20] sky130_fd_sc_hd__clkbuf_4
x1[20] io_out_7_buf[20] vssd1 vssd1 vccd1 vccd1 io_out_7_buf[19] sky130_fd_sc_hd__clkbuf_4
x1[19] io_out_7_buf[19] vssd1 vssd1 vccd1 vccd1 io_out_7_buf[18] sky130_fd_sc_hd__clkbuf_4
x1[18] io_out_7_buf[18] vssd1 vssd1 vccd1 vccd1 io_out_7_buf[17] sky130_fd_sc_hd__clkbuf_4
x1[17] io_out_7_buf[17] vssd1 vssd1 vccd1 vccd1 io_out_7_buf[16] sky130_fd_sc_hd__clkbuf_4
x1[16] io_out_7_buf[16] vssd1 vssd1 vccd1 vccd1 io_out_7_buf[15] sky130_fd_sc_hd__clkbuf_4
x1[15] io_out_7_buf[15] vssd1 vssd1 vccd1 vccd1 io_out_7_buf[14] sky130_fd_sc_hd__clkbuf_4
x1[14] io_out_7_buf[14] vssd1 vssd1 vccd1 vccd1 io_out_7_buf[13] sky130_fd_sc_hd__clkbuf_4
x1[13] io_out_7_buf[13] vssd1 vssd1 vccd1 vccd1 io_out_7_buf[12] sky130_fd_sc_hd__clkbuf_4
x1[12] io_out_7_buf[12] vssd1 vssd1 vccd1 vccd1 io_out_7_buf[11] sky130_fd_sc_hd__clkbuf_4
x1[11] io_out_7_buf[11] vssd1 vssd1 vccd1 vccd1 io_out_7_buf[10] sky130_fd_sc_hd__clkbuf_4
x1[10] io_out_7_buf[10] vssd1 vssd1 vccd1 vccd1 io_out_7_buf[9] sky130_fd_sc_hd__clkbuf_4
x1[9] io_out_7_buf[9] vssd1 vssd1 vccd1 vccd1 io_out_7_buf[8] sky130_fd_sc_hd__clkbuf_4
x1[8] io_out_7_buf[8] vssd1 vssd1 vccd1 vccd1 io_out_7_buf[7] sky130_fd_sc_hd__clkbuf_4
x1[7] io_out_7_buf[7] vssd1 vssd1 vccd1 vccd1 io_out_7_buf[6] sky130_fd_sc_hd__clkbuf_4
x1[6] io_out_7_buf[6] vssd1 vssd1 vccd1 vccd1 io_out_7_buf[5] sky130_fd_sc_hd__clkbuf_4
x1[5] io_out_7_buf[5] vssd1 vssd1 vccd1 vccd1 io_out_7_buf[4] sky130_fd_sc_hd__clkbuf_4
x1[4] io_out_7_buf[4] vssd1 vssd1 vccd1 vccd1 io_out_7_buf[3] sky130_fd_sc_hd__clkbuf_4
x1[3] io_out_7_buf[3] vssd1 vssd1 vccd1 vccd1 io_out_7_buf[2] sky130_fd_sc_hd__clkbuf_4
x1[2] io_out_7_buf[2] vssd1 vssd1 vccd1 vccd1 io_out_7_buf[1] sky130_fd_sc_hd__clkbuf_4
x1[1] io_out_7_buf[1] vssd1 vssd1 vccd1 vccd1 io_out_7_buf[0] sky130_fd_sc_hd__clkbuf_4
x1[0] io_out_7_buf[0] vssd1 vssd1 vccd1 vccd1 io_out[7] sky130_fd_sc_hd__clkbuf_4
x1[14] io_in[10] vssd1 vssd1 vccd1 vccd1 clk_net[14] sky130_fd_sc_hd__clkbuf_4
x1[13] clk_net[14] vssd1 vssd1 vccd1 vccd1 clk_net[13] sky130_fd_sc_hd__clkbuf_4
x1[12] clk_net[13] vssd1 vssd1 vccd1 vccd1 clk_net[12] sky130_fd_sc_hd__clkbuf_4
x1[11] clk_net[12] vssd1 vssd1 vccd1 vccd1 clk_net[11] sky130_fd_sc_hd__clkbuf_4
x1[10] clk_net[11] vssd1 vssd1 vccd1 vccd1 clk_net[10] sky130_fd_sc_hd__clkbuf_4
x1[9] clk_net[10] vssd1 vssd1 vccd1 vccd1 clk_net[9] sky130_fd_sc_hd__clkbuf_4
x1[8] clk_net[9] vssd1 vssd1 vccd1 vccd1 clk_net[8] sky130_fd_sc_hd__clkbuf_4
x1[7] clk_net[8] vssd1 vssd1 vccd1 vccd1 clk_net[7] sky130_fd_sc_hd__clkbuf_4
x1[6] clk_net[7] vssd1 vssd1 vccd1 vccd1 clk_net[6] sky130_fd_sc_hd__clkbuf_4
x1[5] clk_net[6] vssd1 vssd1 vccd1 vccd1 clk_net[5] sky130_fd_sc_hd__clkbuf_4
x1[4] clk_net[5] vssd1 vssd1 vccd1 vccd1 clk_net[4] sky130_fd_sc_hd__clkbuf_4
x1[3] clk_net[4] vssd1 vssd1 vccd1 vccd1 clk_net[3] sky130_fd_sc_hd__clkbuf_4
x1[2] clk_net[3] vssd1 vssd1 vccd1 vccd1 clk_net[2] sky130_fd_sc_hd__clkbuf_4
x1[1] clk_net[2] vssd1 vssd1 vccd1 vccd1 clk_net[1] sky130_fd_sc_hd__clkbuf_4
x1[0] clk_net[1] vssd1 vssd1 vccd1 vccd1 clk_net[0] sky130_fd_sc_hd__clkbuf_4
x4 clk_net[0] vssd1 vssd1 vccd1 vccd1 net1 sky130_fd_sc_hd__clkbuf_4
x3 clk_net[0] vssd1 vssd1 vccd1 vccd1 net2 sky130_fd_sc_hd__clkbuf_4
x5 net1 vssd1 vssd1 vccd1 vccd1 net3 sky130_fd_sc_hd__clkbuf_4
x6 net3 vssd1 vssd1 vccd1 vccd1 net4 sky130_fd_sc_hd__clkbuf_4
x7 net4 vssd1 vssd1 vccd1 vccd1 net5 sky130_fd_sc_hd__clkbuf_4
x8 net5 vssd1 vssd1 vccd1 vccd1 net6 sky130_fd_sc_hd__clkbuf_4
x9 net6 vssd1 vssd1 vccd1 vccd1 df_clk sky130_fd_sc_hd__clkbuf_4
x10 net2 vssd1 vssd1 vccd1 vccd1 net7 sky130_fd_sc_hd__clkbuf_4
x11 net7 vssd1 vssd1 vccd1 vccd1 net8 sky130_fd_sc_hd__clkbuf_4
x12 net8 vssd1 vssd1 vccd1 vccd1 net9 sky130_fd_sc_hd__clkbuf_4
x13 net9 vssd1 vssd1 vccd1 vccd1 net10 sky130_fd_sc_hd__clkbuf_4
x14 net10 vssd1 vssd1 vccd1 vccd1 mod_clk sky130_fd_sc_hd__clkbuf_4
x2[14] io_in[9] vssd1 vssd1 vccd1 vccd1 rst_net[14] sky130_fd_sc_hd__clkbuf_4
x2[13] rst_net[14] vssd1 vssd1 vccd1 vccd1 rst_net[13] sky130_fd_sc_hd__clkbuf_4
x2[12] rst_net[13] vssd1 vssd1 vccd1 vccd1 rst_net[12] sky130_fd_sc_hd__clkbuf_4
x2[11] rst_net[12] vssd1 vssd1 vccd1 vccd1 rst_net[11] sky130_fd_sc_hd__clkbuf_4
x2[10] rst_net[11] vssd1 vssd1 vccd1 vccd1 rst_net[10] sky130_fd_sc_hd__clkbuf_4
x2[9] rst_net[10] vssd1 vssd1 vccd1 vccd1 rst_net[9] sky130_fd_sc_hd__clkbuf_4
x2[8] rst_net[9] vssd1 vssd1 vccd1 vccd1 rst_net[8] sky130_fd_sc_hd__clkbuf_4
x2[7] rst_net[8] vssd1 vssd1 vccd1 vccd1 rst_net[7] sky130_fd_sc_hd__clkbuf_4
x2[6] rst_net[7] vssd1 vssd1 vccd1 vccd1 rst_net[6] sky130_fd_sc_hd__clkbuf_4
x2[5] rst_net[6] vssd1 vssd1 vccd1 vccd1 rst_net[5] sky130_fd_sc_hd__clkbuf_4
x2[4] rst_net[5] vssd1 vssd1 vccd1 vccd1 rst_net[4] sky130_fd_sc_hd__clkbuf_4
x2[3] rst_net[4] vssd1 vssd1 vccd1 vccd1 rst_net[3] sky130_fd_sc_hd__clkbuf_4
x2[2] rst_net[3] vssd1 vssd1 vccd1 vccd1 rst_net[2] sky130_fd_sc_hd__clkbuf_4
x2[1] rst_net[2] vssd1 vssd1 vccd1 vccd1 rst_net[1] sky130_fd_sc_hd__clkbuf_4
x2[0] rst_net[1] vssd1 vssd1 vccd1 vccd1 rst_net[0] sky130_fd_sc_hd__clkbuf_4
x15 rst_net[0] vssd1 vssd1 vccd1 vccd1 net11 sky130_fd_sc_hd__clkbuf_4
x16 rst_net[0] vssd1 vssd1 vccd1 vccd1 net12 sky130_fd_sc_hd__clkbuf_4
x17 net11 vssd1 vssd1 vccd1 vccd1 net13 sky130_fd_sc_hd__clkbuf_4
x18 net13 vssd1 vssd1 vccd1 vccd1 net14 sky130_fd_sc_hd__clkbuf_4
x19 net14 vssd1 vssd1 vccd1 vccd1 net15 sky130_fd_sc_hd__clkbuf_4
x20 net15 vssd1 vssd1 vccd1 vccd1 net16 sky130_fd_sc_hd__clkbuf_4
x21 net16 vssd1 vssd1 vccd1 vccd1 net17 sky130_fd_sc_hd__clkbuf_4
x22 net12 vssd1 vssd1 vccd1 vccd1 net18 sky130_fd_sc_hd__clkbuf_4
x23 net18 vssd1 vssd1 vccd1 vccd1 net19 sky130_fd_sc_hd__clkbuf_4
x24 net19 vssd1 vssd1 vccd1 vccd1 net20 sky130_fd_sc_hd__clkbuf_4
x25 net20 vssd1 vssd1 vccd1 vccd1 net21 sky130_fd_sc_hd__clkbuf_4
x26 net21 vssd1 vssd1 vccd1 vccd1 mod_rst sky130_fd_sc_hd__clkbuf_4
x27 net17 vssd1 vssd1 vccd1 vccd1 df_rst sky130_fd_sc_hd__clkbuf_4
XC1 vccd1 vssd1 sky130_fd_pr__cap_mim_m3_1 W=29.99 L=29.99 MF=96 m=96
x2[20] io_out_13_buf[20] vssd1 vssd1 vccd1 vccd1 io_out_13_buf[19] sky130_fd_sc_hd__clkbuf_4
x2[19] io_out_13_buf[19] vssd1 vssd1 vccd1 vccd1 io_out_13_buf[18] sky130_fd_sc_hd__clkbuf_4
x2[18] io_out_13_buf[18] vssd1 vssd1 vccd1 vccd1 io_out_13_buf[17] sky130_fd_sc_hd__clkbuf_4
x2[17] io_out_13_buf[17] vssd1 vssd1 vccd1 vccd1 io_out_13_buf[16] sky130_fd_sc_hd__clkbuf_4
x2[16] io_out_13_buf[16] vssd1 vssd1 vccd1 vccd1 io_out_13_buf[15] sky130_fd_sc_hd__clkbuf_4
x2[15] io_out_13_buf[15] vssd1 vssd1 vccd1 vccd1 io_out_13_buf[14] sky130_fd_sc_hd__clkbuf_4
x2[14] io_out_13_buf[14] vssd1 vssd1 vccd1 vccd1 io_out_13_buf[13] sky130_fd_sc_hd__clkbuf_4
x2[13] io_out_13_buf[13] vssd1 vssd1 vccd1 vccd1 io_out_13_buf[12] sky130_fd_sc_hd__clkbuf_4
x2[12] io_out_13_buf[12] vssd1 vssd1 vccd1 vccd1 io_out_13_buf[11] sky130_fd_sc_hd__clkbuf_4
x2[11] io_out_13_buf[11] vssd1 vssd1 vccd1 vccd1 io_out_13_buf[10] sky130_fd_sc_hd__clkbuf_4
x2[10] io_out_13_buf[10] vssd1 vssd1 vccd1 vccd1 io_out_13_buf[9] sky130_fd_sc_hd__clkbuf_4
x2[9] io_out_13_buf[9] vssd1 vssd1 vccd1 vccd1 io_out_13_buf[8] sky130_fd_sc_hd__clkbuf_4
x2[8] io_out_13_buf[8] vssd1 vssd1 vccd1 vccd1 io_out_13_buf[7] sky130_fd_sc_hd__clkbuf_4
x2[7] io_out_13_buf[7] vssd1 vssd1 vccd1 vccd1 io_out_13_buf[6] sky130_fd_sc_hd__clkbuf_4
x2[6] io_out_13_buf[6] vssd1 vssd1 vccd1 vccd1 io_out_13_buf[5] sky130_fd_sc_hd__clkbuf_4
x2[5] io_out_13_buf[5] vssd1 vssd1 vccd1 vccd1 io_out_13_buf[4] sky130_fd_sc_hd__clkbuf_4
x2[4] io_out_13_buf[4] vssd1 vssd1 vccd1 vccd1 io_out_13_buf[3] sky130_fd_sc_hd__clkbuf_4
x2[3] io_out_13_buf[3] vssd1 vssd1 vccd1 vccd1 io_out_13_buf[2] sky130_fd_sc_hd__clkbuf_4
x2[2] io_out_13_buf[2] vssd1 vssd1 vccd1 vccd1 io_out_13_buf[1] sky130_fd_sc_hd__clkbuf_4
x2[1] io_out_13_buf[1] vssd1 vssd1 vccd1 vccd1 io_out_13_buf[0] sky130_fd_sc_hd__clkbuf_4
x2[0] io_out_13_buf[0] vssd1 vssd1 vccd1 vccd1 io_out[13] sky130_fd_sc_hd__clkbuf_4
x1[20] io_in[12] vssd1 vssd1 vccd1 vccd1 io_in_12_buf[20] sky130_fd_sc_hd__clkbuf_4
x1[19] io_in_12_buf[20] vssd1 vssd1 vccd1 vccd1 io_in_12_buf[19] sky130_fd_sc_hd__clkbuf_4
x1[18] io_in_12_buf[19] vssd1 vssd1 vccd1 vccd1 io_in_12_buf[18] sky130_fd_sc_hd__clkbuf_4
x1[17] io_in_12_buf[18] vssd1 vssd1 vccd1 vccd1 io_in_12_buf[17] sky130_fd_sc_hd__clkbuf_4
x1[16] io_in_12_buf[17] vssd1 vssd1 vccd1 vccd1 io_in_12_buf[16] sky130_fd_sc_hd__clkbuf_4
x1[15] io_in_12_buf[16] vssd1 vssd1 vccd1 vccd1 io_in_12_buf[15] sky130_fd_sc_hd__clkbuf_4
x1[14] io_in_12_buf[15] vssd1 vssd1 vccd1 vccd1 io_in_12_buf[14] sky130_fd_sc_hd__clkbuf_4
x1[13] io_in_12_buf[14] vssd1 vssd1 vccd1 vccd1 io_in_12_buf[13] sky130_fd_sc_hd__clkbuf_4
x1[12] io_in_12_buf[13] vssd1 vssd1 vccd1 vccd1 io_in_12_buf[12] sky130_fd_sc_hd__clkbuf_4
x1[11] io_in_12_buf[12] vssd1 vssd1 vccd1 vccd1 io_in_12_buf[11] sky130_fd_sc_hd__clkbuf_4
x1[10] io_in_12_buf[11] vssd1 vssd1 vccd1 vccd1 io_in_12_buf[10] sky130_fd_sc_hd__clkbuf_4
x1[9] io_in_12_buf[10] vssd1 vssd1 vccd1 vccd1 io_in_12_buf[9] sky130_fd_sc_hd__clkbuf_4
x1[8] io_in_12_buf[9] vssd1 vssd1 vccd1 vccd1 io_in_12_buf[8] sky130_fd_sc_hd__clkbuf_4
x1[7] io_in_12_buf[8] vssd1 vssd1 vccd1 vccd1 io_in_12_buf[7] sky130_fd_sc_hd__clkbuf_4
x1[6] io_in_12_buf[7] vssd1 vssd1 vccd1 vccd1 io_in_12_buf[6] sky130_fd_sc_hd__clkbuf_4
x1[5] io_in_12_buf[6] vssd1 vssd1 vccd1 vccd1 io_in_12_buf[5] sky130_fd_sc_hd__clkbuf_4
x1[4] io_in_12_buf[5] vssd1 vssd1 vccd1 vccd1 io_in_12_buf[4] sky130_fd_sc_hd__clkbuf_4
x1[3] io_in_12_buf[4] vssd1 vssd1 vccd1 vccd1 io_in_12_buf[3] sky130_fd_sc_hd__clkbuf_4
x1[2] io_in_12_buf[3] vssd1 vssd1 vccd1 vccd1 io_in_12_buf[2] sky130_fd_sc_hd__clkbuf_4
x1[1] io_in_12_buf[2] vssd1 vssd1 vccd1 vccd1 io_in_12_buf[1] sky130_fd_sc_hd__clkbuf_4
x1[0] io_in_12_buf[1] vssd1 vssd1 vccd1 vccd1 io_in_12_buf[0] sky130_fd_sc_hd__clkbuf_4
x3[20] io_in[11] vssd1 vssd1 vccd1 vccd1 io_in_11_buf[20] sky130_fd_sc_hd__clkbuf_4
x3[19] io_in_11_buf[20] vssd1 vssd1 vccd1 vccd1 io_in_11_buf[19] sky130_fd_sc_hd__clkbuf_4
x3[18] io_in_11_buf[19] vssd1 vssd1 vccd1 vccd1 io_in_11_buf[18] sky130_fd_sc_hd__clkbuf_4
x3[17] io_in_11_buf[18] vssd1 vssd1 vccd1 vccd1 io_in_11_buf[17] sky130_fd_sc_hd__clkbuf_4
x3[16] io_in_11_buf[17] vssd1 vssd1 vccd1 vccd1 io_in_11_buf[16] sky130_fd_sc_hd__clkbuf_4
x3[15] io_in_11_buf[16] vssd1 vssd1 vccd1 vccd1 io_in_11_buf[15] sky130_fd_sc_hd__clkbuf_4
x3[14] io_in_11_buf[15] vssd1 vssd1 vccd1 vccd1 io_in_11_buf[14] sky130_fd_sc_hd__clkbuf_4
x3[13] io_in_11_buf[14] vssd1 vssd1 vccd1 vccd1 io_in_11_buf[13] sky130_fd_sc_hd__clkbuf_4
x3[12] io_in_11_buf[13] vssd1 vssd1 vccd1 vccd1 io_in_11_buf[12] sky130_fd_sc_hd__clkbuf_4
x3[11] io_in_11_buf[12] vssd1 vssd1 vccd1 vccd1 io_in_11_buf[11] sky130_fd_sc_hd__clkbuf_4
x3[10] io_in_11_buf[11] vssd1 vssd1 vccd1 vccd1 io_in_11_buf[10] sky130_fd_sc_hd__clkbuf_4
x3[9] io_in_11_buf[10] vssd1 vssd1 vccd1 vccd1 io_in_11_buf[9] sky130_fd_sc_hd__clkbuf_4
x3[8] io_in_11_buf[9] vssd1 vssd1 vccd1 vccd1 io_in_11_buf[8] sky130_fd_sc_hd__clkbuf_4
x3[7] io_in_11_buf[8] vssd1 vssd1 vccd1 vccd1 io_in_11_buf[7] sky130_fd_sc_hd__clkbuf_4
x3[6] io_in_11_buf[7] vssd1 vssd1 vccd1 vccd1 io_in_11_buf[6] sky130_fd_sc_hd__clkbuf_4
x3[5] io_in_11_buf[6] vssd1 vssd1 vccd1 vccd1 io_in_11_buf[5] sky130_fd_sc_hd__clkbuf_4
x3[4] io_in_11_buf[5] vssd1 vssd1 vccd1 vccd1 io_in_11_buf[4] sky130_fd_sc_hd__clkbuf_4
x3[3] io_in_11_buf[4] vssd1 vssd1 vccd1 vccd1 io_in_11_buf[3] sky130_fd_sc_hd__clkbuf_4
x3[2] io_in_11_buf[3] vssd1 vssd1 vccd1 vccd1 io_in_11_buf[2] sky130_fd_sc_hd__clkbuf_4
x3[1] io_in_11_buf[2] vssd1 vssd1 vccd1 vccd1 io_in_11_buf[1] sky130_fd_sc_hd__clkbuf_4
x3[0] io_in_11_buf[1] vssd1 vssd1 vccd1 vccd1 io_in_11_buf[0] sky130_fd_sc_hd__clkbuf_4
x1 mod_clk io_analog[10] io_analog[9] mod_rst io_analog[8] io_analog[1] la_data_in[101]
+ la_data_in[100] la_data_in[99] la_data_in[63] la_data_in[62] la_data_in[65] la_data_in[64] io_out_7_buf[23]
+ io_analog[2] io_analog[0] io_analog[7] io_analog[3] io_out_26_buf[38] la_data_in[61] la_data_in[60] vccd1 vssd1
+ analog_top
**.ends
.end
